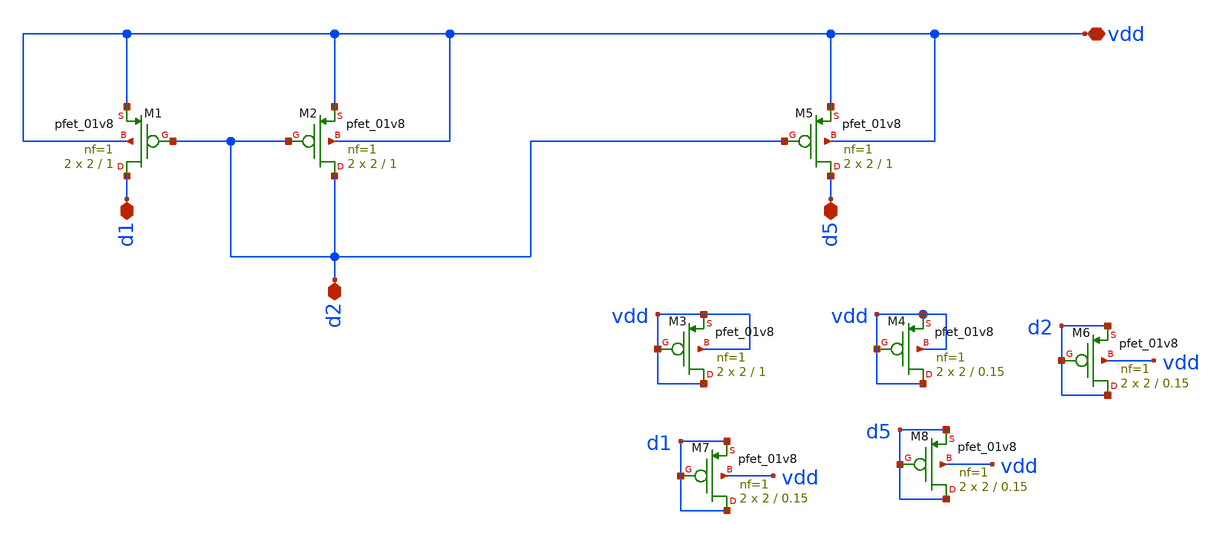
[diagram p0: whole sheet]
** sch_path: opamp/mag/pmoscs.sch
**.subckt pmoscs vdd d5 d2 d1
*.iopin vdd
*.iopin d5
*.iopin d2
*.iopin d1
XM1 d1 d2 vdd vdd sky130_fd_pr__pfet_01v8 L=1 W=2 nf=1 ad='int((nf+1)/2) * W/nf * 0.29' as='int((nf+2)/2) * W/nf * 0.29'
+ pd='2*int((nf+1)/2) * (W/nf + 0.29)' ps='2*int((nf+2)/2) * (W/nf + 0.29)' nrd='0.29 / W' nrs='0.29 / W'
+ sa=0 sb=0 sd=0 mult=2 m=2
XM5 d5 d2 vdd vdd sky130_fd_pr__pfet_01v8 L=1 W=2 nf=1 ad='int((nf+1)/2) * W/nf * 0.29' as='int((nf+2)/2) * W/nf * 0.29'
+ pd='2*int((nf+1)/2) * (W/nf + 0.29)' ps='2*int((nf+2)/2) * (W/nf + 0.29)' nrd='0.29 / W' nrs='0.29 / W'
+ sa=0 sb=0 sd=0 mult=2 m=2
XM2 d2 d2 vdd vdd sky130_fd_pr__pfet_01v8 L=1 W=2 nf=1 ad='int((nf+1)/2) * W/nf * 0.29' as='int((nf+2)/2) * W/nf * 0.29'
+ pd='2*int((nf+1)/2) * (W/nf + 0.29)' ps='2*int((nf+2)/2) * (W/nf + 0.29)' nrd='0.29 / W' nrs='0.29 / W'
+ sa=0 sb=0 sd=0 mult=2 m=2
XM3 vdd vdd vdd vdd sky130_fd_pr__pfet_01v8 L=1 W=2 nf=1 ad='int((nf+1)/2) * W/nf * 0.29' as='int((nf+2)/2) * W/nf * 0.29'
+ pd='2*int((nf+1)/2) * (W/nf + 0.29)' ps='2*int((nf+2)/2) * (W/nf + 0.29)' nrd='0.29 / W' nrs='0.29 / W'
+ sa=0 sb=0 sd=0 mult=2 m=2
XM4 vdd vdd vdd vdd sky130_fd_pr__pfet_01v8 L=0.15 W=2 nf=1 ad='int((nf+1)/2) * W/nf * 0.29' as='int((nf+2)/2) * W/nf * 0.29'
+ pd='2*int((nf+1)/2) * (W/nf + 0.29)' ps='2*int((nf+2)/2) * (W/nf + 0.29)' nrd='0.29 / W' nrs='0.29 / W'
+ sa=0 sb=0 sd=0 mult=2 m=2
XM6 d2 d2 d2 vdd sky130_fd_pr__pfet_01v8 L=0.15 W=2 nf=1 ad='int((nf+1)/2) * W/nf * 0.29' as='int((nf+2)/2) * W/nf * 0.29'
+ pd='2*int((nf+1)/2) * (W/nf + 0.29)' ps='2*int((nf+2)/2) * (W/nf + 0.29)' nrd='0.29 / W' nrs='0.29 / W'
+ sa=0 sb=0 sd=0 mult=2 m=2
XM7 d1 d1 d1 vdd sky130_fd_pr__pfet_01v8 L=0.15 W=2 nf=1 ad='int((nf+1)/2) * W/nf * 0.29' as='int((nf+2)/2) * W/nf * 0.29'
+ pd='2*int((nf+1)/2) * (W/nf + 0.29)' ps='2*int((nf+2)/2) * (W/nf + 0.29)' nrd='0.29 / W' nrs='0.29 / W'
+ sa=0 sb=0 sd=0 mult=2 m=2
XM8 d5 d5 d5 vdd sky130_fd_pr__pfet_01v8 L=0.15 W=2 nf=1 ad='int((nf+1)/2) * W/nf * 0.29' as='int((nf+2)/2) * W/nf * 0.29'
+ pd='2*int((nf+1)/2) * (W/nf + 0.29)' ps='2*int((nf+2)/2) * (W/nf + 0.29)' nrd='0.29 / W' nrs='0.29 / W'
+ sa=0 sb=0 sd=0 mult=2 m=2
**.ends
.end
